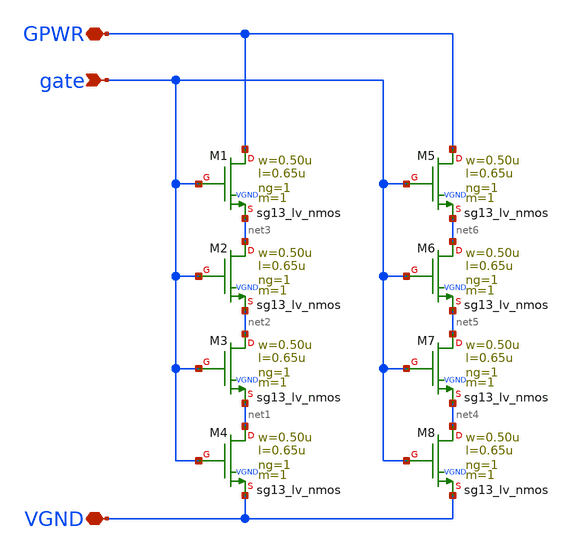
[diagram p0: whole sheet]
** sch_path: pg/ihp-sg13cmos5l/common/xschem/discharge_1v5.sch
**.subckt discharge_1v5 GPWR VGND gate
*.iopin GPWR
*.iopin VGND
*.ipin gate
XM1 GPWR gate net3 VGND sg13_lv_nmos w=0.50u l=0.65u ng=1 m=1
XM2 net3 gate net2 VGND sg13_lv_nmos w=0.50u l=0.65u ng=1 m=1
XM3 net2 gate net1 VGND sg13_lv_nmos w=0.50u l=0.65u ng=1 m=1
XM4 net1 gate VGND VGND sg13_lv_nmos w=0.50u l=0.65u ng=1 m=1
XM5 GPWR gate net6 VGND sg13_lv_nmos w=0.50u l=0.65u ng=1 m=1
XM6 net6 gate net5 VGND sg13_lv_nmos w=0.50u l=0.65u ng=1 m=1
XM7 net5 gate net4 VGND sg13_lv_nmos w=0.50u l=0.65u ng=1 m=1
XM8 net4 gate VGND VGND sg13_lv_nmos w=0.50u l=0.65u ng=1 m=1
**.ends
.end
